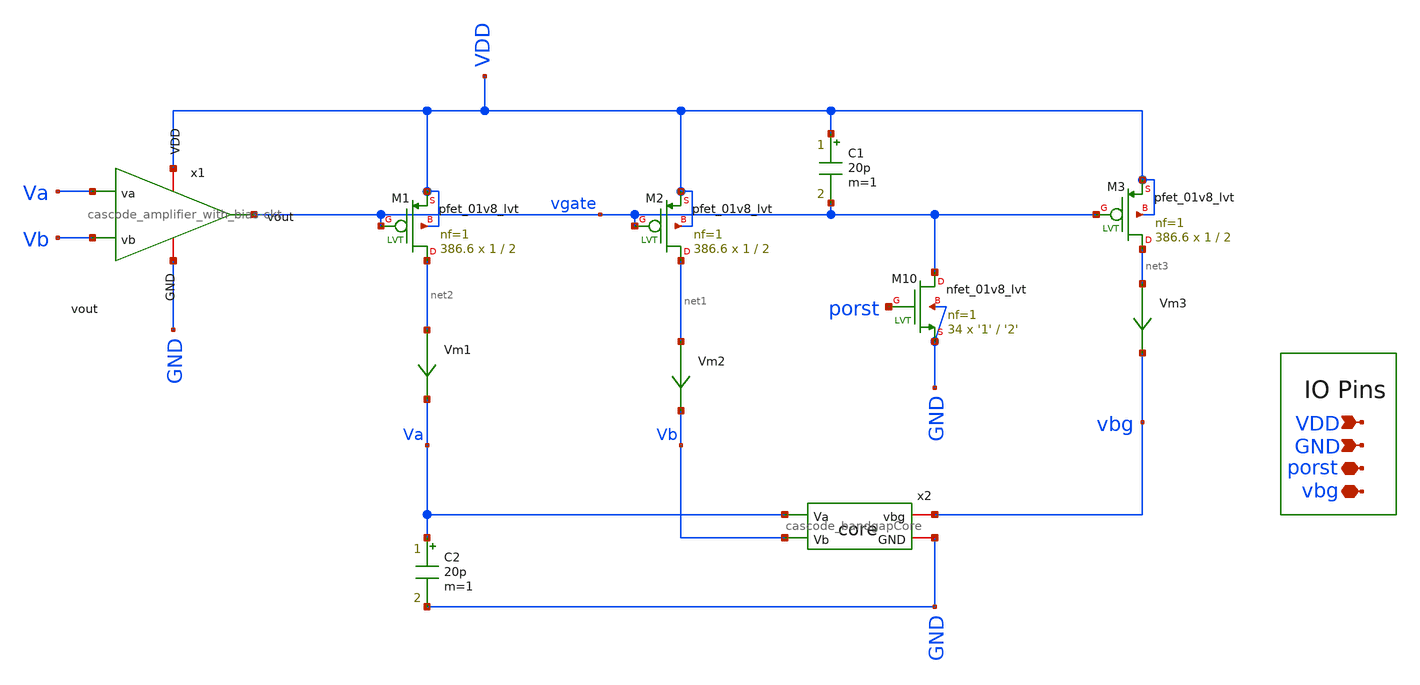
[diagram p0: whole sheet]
** sch_path: bandgap_sky130_v1/bandgap_top.sch
**.subckt bandgap_top VDD GND porst vbg
*.ipin VDD
*.ipin GND
*.iopin porst
*.iopin vbg
x1 Va Vb vgate VDD GND cascode_amplifier_with_bias-ckt
x2 Va Vb vbg GND cascode_bandgapCore
Vm1 net2 Va 0
.save i(vm1)
Vm2 net1 Vb 0
.save i(vm2)
Vm3 net3 vbg 0
.save i(vm3)
XM1 net2 vgate VDD VDD sky130_fd_pr__pfet_01v8_lvt L=2 W=1 nf=1 ad='int((nf+1)/2) * W/nf * 0.29' as='int((nf+2)/2) * W/nf * 0.29'
+ pd='2*int((nf+1)/2) * (W/nf + 0.29)' ps='2*int((nf+2)/2) * (W/nf + 0.29)' nrd='0.29 / W' nrs='0.29 / W'
+ sa=0 sb=0 sd=0 mult=386.6 m=386.6
XM2 net1 vgate VDD VDD sky130_fd_pr__pfet_01v8_lvt L=2 W=1 nf=1 ad='int((nf+1)/2) * W/nf * 0.29' as='int((nf+2)/2) * W/nf * 0.29'
+ pd='2*int((nf+1)/2) * (W/nf + 0.29)' ps='2*int((nf+2)/2) * (W/nf + 0.29)' nrd='0.29 / W' nrs='0.29 / W'
+ sa=0 sb=0 sd=0 mult=386.6 m=386.6
XM3 net3 vgate VDD VDD sky130_fd_pr__pfet_01v8_lvt L=2 W=1 nf=1 ad='int((nf+1)/2) * W/nf * 0.29' as='int((nf+2)/2) * W/nf * 0.29'
+ pd='2*int((nf+1)/2) * (W/nf + 0.29)' ps='2*int((nf+2)/2) * (W/nf + 0.29)' nrd='0.29 / W' nrs='0.29 / W'
+ sa=0 sb=0 sd=0 mult=386.6 m=386.6
XM10 vgate porst GND GND sky130_fd_pr__nfet_01v8_lvt L='2' W='1' nf=1 ad='int((nf+1)/2) * W/nf * 0.29'
+ as='int((nf+2)/2) * W/nf * 0.29' pd='2*int((nf+1)/2) * (W/nf + 0.29)' ps='2*int((nf+2)/2) * (W/nf + 0.29)'
+ nrd='0.29 / W' nrs='0.29 / W' sa=0 sb=0 sd=0 mult=34 m=34
C1 VDD vgate 20p m=1
C2 Va GND 20p m=1
**.ends
.end
